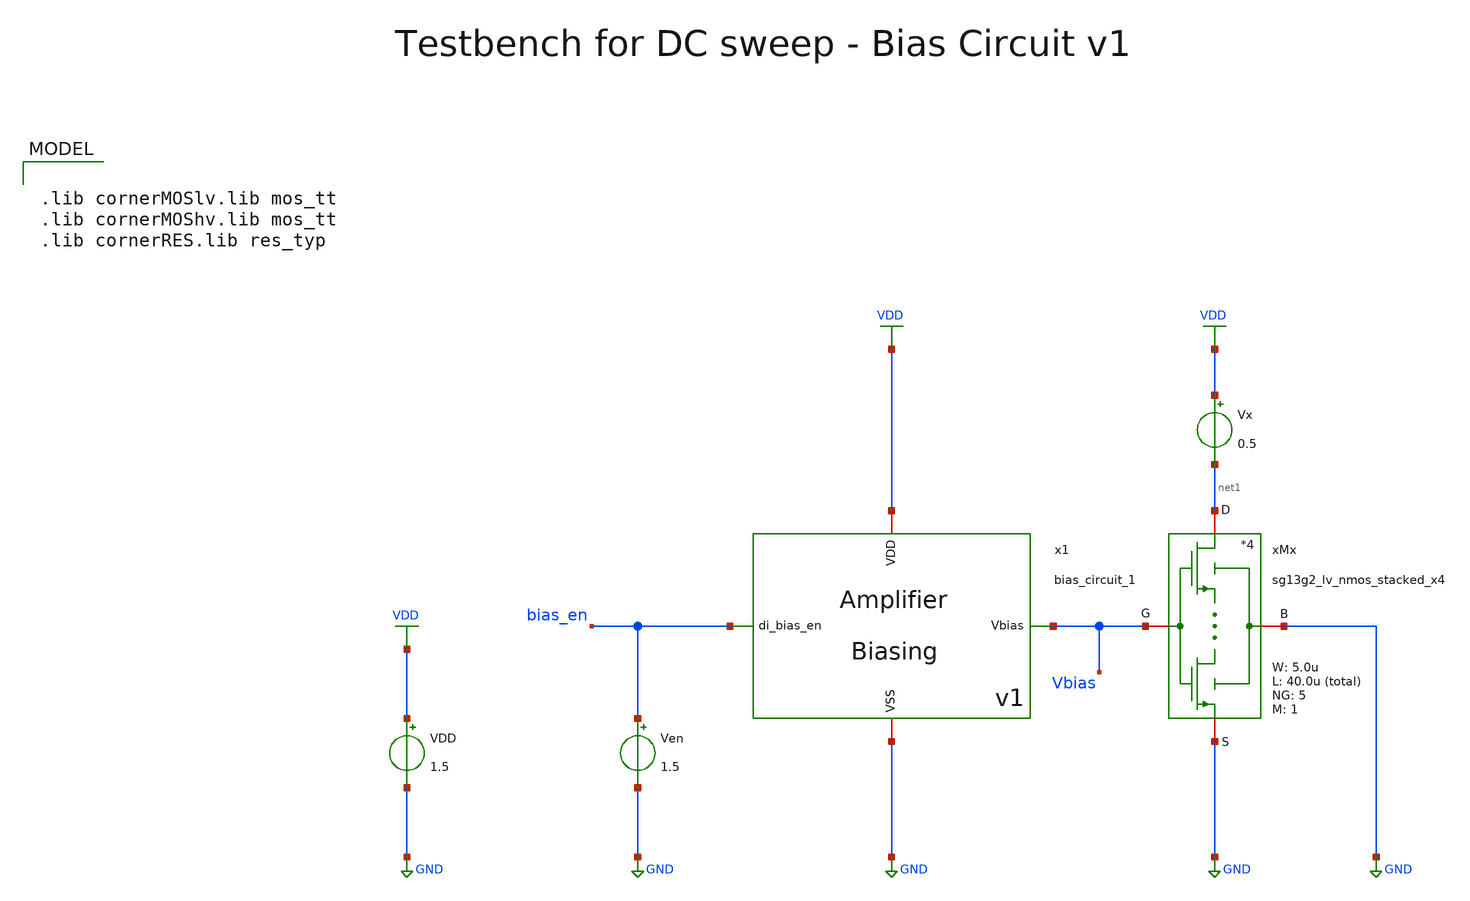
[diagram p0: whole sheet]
** sch_path: SG13G2_ATBS-ADC-main/xschem/bio_amplifier/amplifier_core/bias_circuit/bias_circuit_1/testbenches/bias_circuit_1_tb_dc.sch
**.subckt bias_circuit_1_tb_dc
Ven bias_en GND 1.5
VDD VDD GND 1.5
xMx net1 Vbias GND GND sg13g2_lv_nmos_stacked_x4 W_N=5.0u L_N=40.0u NG_N=5 M_N=1
Vx VDD net1 0.5
x1 bias_en Vbias VDD GND bias_circuit_1
**** begin user architecture code

.lib cornerMOSlv.lib mos_tt
.lib cornerMOShv.lib mos_tt
.lib cornerRES.lib res_typ



.param temp=27
.options savecurrents reltol=1e-3 abstol=1e-15 gmin=1e-15
.control

save all

* Operating Point Analysis
op
remzerovec
write bias_circuit_1_tb_dc.raw
set appendwrite

* DC Sweep of Vout
dc Vx 0 1.5 5m
remzerovec
write bias_circuit_1_tb_dc.raw

* Plotting
plot i(Vx) xlabel Vx

* Measurements
meas dc Ix_1V FIND i(Vx) at=1
meas dc Ix_0V FIND i(Vx) at=0
let Ix_volt = Ix_0V - Ix_1V
print Ix_volt

* DC Sweep of VDD
dc VDD 0 1.5 5m
remzerovec
write bias_circuit_1_tb_dc.raw

* Plotting
plot v(Vbias) xlabel VDD
plot i(Vx) xlabel VDD
plot i(v.x1.viref) i(v.x1.viout) xlabel VDD

* Measurements
let Iout_nominal = 10e-9
let Iout_99_percent = 0.99 * Iout_nominal
print Iout_99_percent
meas dc VDD_min WHEN i(v.x1.viout)=Iout_99_percent

meas dc Iout_1_5V FIND i(v.x1.viout) at=1.49
meas dc Iout_1_4V FIND i(v.x1.viout) at=1.39
let Iout_volt = (Iout_1_5V - Iout_1_4V) * 10
print Iout_volt

* Write Data
set wr_vecnames
set wr_singlescale
let Ix=i(Vx)
let Iout=i(v.x1.viout)
wrdata /foss/designs/SG13G2_ATBS-ADC-main/python/plot_simulations/data/bias_circuit_1_tb_dc.txt
+ v(Vbias) v(Ix) v(Iout)

*quit
.endc

**** end user architecture code
**.ends
.GLOBAL GND
.GLOBAL VDD
.end
